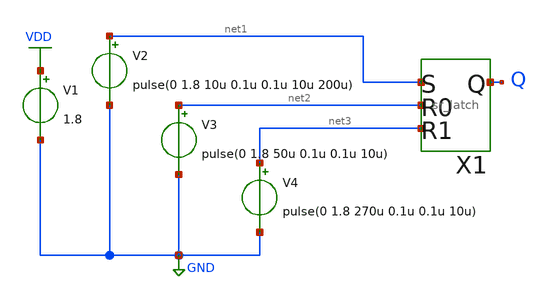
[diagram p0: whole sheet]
** sch_path: xschem/sr_latch_tb.sch
**.subckt sr_latch_tb
X1 net1 net2 Q net3 sr_latch
V1 VDD GND 1.8
V2 net1 GND pulse(0 1.8 10u 0.1u 0.1u 10u 200u)
V3 net2 GND pulse(0 1.8 50u 0.1u 0.1u 10u)
V4 net3 GND pulse(0 1.8 270u 0.1u 0.1u 10u)
**** begin user architecture code


.option wnflag=1
.lib /usr/local/share/pdk/sky130A/libs.tech/ngspice/sky130.lib.spice tt
.tran 0.05u 300u
.save all


**** end user architecture code
**.ends

* expanding   symbol:  sr_latch.sym # of pins=4
** sym_path: xschem/sr_latch.sym
** sch_path: xschem/sr_latch.sch
.subckt sr_latch s r0 q r1
*.ipin s
*.ipin r0
*.opin q
*.ipin r1
XM1 net1 q net2 VDD sky130_fd_pr__pfet_01v8 L=0.15 W=1 nf=1 ad='int((1 + 1)/2) * 1 / 1 * 0.29' as='int((1 + 2)/2) * 1 / 1 * 0.29'
+ pd='2*int((1 + 1)/2) * (1 / 1 + 0.29)' ps='2*int((1 + 2)/2) * (1 / 1 + 0.29)' nrd='0.29 / 1 ' nrs='0.29 / 1 '
+ sa=0 sb=0 sd=0 mult=1 m=1
XM2 net2 s VDD VDD sky130_fd_pr__pfet_01v8 L=0.15 W=1 nf=1 ad='int((1 + 1)/2) * 1 / 1 * 0.29' as='int((1 + 2)/2) * 1 / 1 * 0.29'
+ pd='2*int((1 + 1)/2) * (1 / 1 + 0.29)' ps='2*int((1 + 2)/2) * (1 / 1 + 0.29)' nrd='0.29 / 1 ' nrs='0.29 / 1 '
+ sa=0 sb=0 sd=0 mult=1 m=1
XM3 net1 s GND GND sky130_fd_pr__nfet_01v8 L=0.15 W=1 nf=1 ad='int((1 + 1)/2) * 1 / 1 * 0.29' as='int((1 + 2)/2) * 1 / 1 * 0.29'
+ pd='2*int((1 + 1)/2) * (1 / 1 + 0.29)' ps='2*int((1 + 2)/2) * (1 / 1 + 0.29)' nrd='0.29 / 1 ' nrs='0.29 / 1 '
+ sa=0 sb=0 sd=0 mult=1 m=1
XM4 net1 q GND GND sky130_fd_pr__nfet_01v8 L=0.15 W=1 nf=1 ad='int((1 + 1)/2) * 1 / 1 * 0.29' as='int((1 + 2)/2) * 1 / 1 * 0.29'
+ pd='2*int((1 + 1)/2) * (1 / 1 + 0.29)' ps='2*int((1 + 2)/2) * (1 / 1 + 0.29)' nrd='0.29 / 1 ' nrs='0.29 / 1 '
+ sa=0 sb=0 sd=0 mult=1 m=1
XM5 q net1 net3 VDD sky130_fd_pr__pfet_01v8 L=0.15 W=1 nf=1 ad='int((1 + 1)/2) * 1 / 1 * 0.29' as='int((1 + 2)/2) * 1 / 1 * 0.29'
+ pd='2*int((1 + 1)/2) * (1 / 1 + 0.29)' ps='2*int((1 + 2)/2) * (1 / 1 + 0.29)' nrd='0.29 / 1 ' nrs='0.29 / 1 '
+ sa=0 sb=0 sd=0 mult=1 m=1
XM6 net3 r0 net4 VDD sky130_fd_pr__pfet_01v8 L=0.15 W=1 nf=1 ad='int((1 + 1)/2) * 1 / 1 * 0.29' as='int((1 + 2)/2) * 1 / 1 * 0.29'
+ pd='2*int((1 + 1)/2) * (1 / 1 + 0.29)' ps='2*int((1 + 2)/2) * (1 / 1 + 0.29)' nrd='0.29 / 1 ' nrs='0.29 / 1 '
+ sa=0 sb=0 sd=0 mult=1 m=1
XM7 q r0 GND GND sky130_fd_pr__nfet_01v8 L=0.15 W=1 nf=1 ad='int((1 + 1)/2) * 1 / 1 * 0.29' as='int((1 + 2)/2) * 1 / 1 * 0.29'
+ pd='2*int((1 + 1)/2) * (1 / 1 + 0.29)' ps='2*int((1 + 2)/2) * (1 / 1 + 0.29)' nrd='0.29 / 1 ' nrs='0.29 / 1 '
+ sa=0 sb=0 sd=0 mult=1 m=1
XM8 q net1 GND GND sky130_fd_pr__nfet_01v8 L=0.15 W=1 nf=1 ad='int((1 + 1)/2) * 1 / 1 * 0.29' as='int((1 + 2)/2) * 1 / 1 * 0.29'
+ pd='2*int((1 + 1)/2) * (1 / 1 + 0.29)' ps='2*int((1 + 2)/2) * (1 / 1 + 0.29)' nrd='0.29 / 1 ' nrs='0.29 / 1 '
+ sa=0 sb=0 sd=0 mult=1 m=1
XM9 net4 r1 VDD VDD sky130_fd_pr__pfet_01v8 L=0.15 W=1 nf=1 ad='int((1 + 1)/2) * 1 / 1 * 0.29' as='int((1 + 2)/2) * 1 / 1 * 0.29'
+ pd='2*int((1 + 1)/2) * (1 / 1 + 0.29)' ps='2*int((1 + 2)/2) * (1 / 1 + 0.29)' nrd='0.29 / 1 ' nrs='0.29 / 1 '
+ sa=0 sb=0 sd=0 mult=1 m=1
XM10 q r1 GND GND sky130_fd_pr__nfet_01v8 L=0.15 W=1 nf=1 ad='int((1 + 1)/2) * 1 / 1 * 0.29' as='int((1 + 2)/2) * 1 / 1 * 0.29'
+ pd='2*int((1 + 1)/2) * (1 / 1 + 0.29)' ps='2*int((1 + 2)/2) * (1 / 1 + 0.29)' nrd='0.29 / 1 ' nrs='0.29 / 1 '
+ sa=0 sb=0 sd=0 mult=1 m=1
.ends

.GLOBAL VDD
.GLOBAL GND
.end
